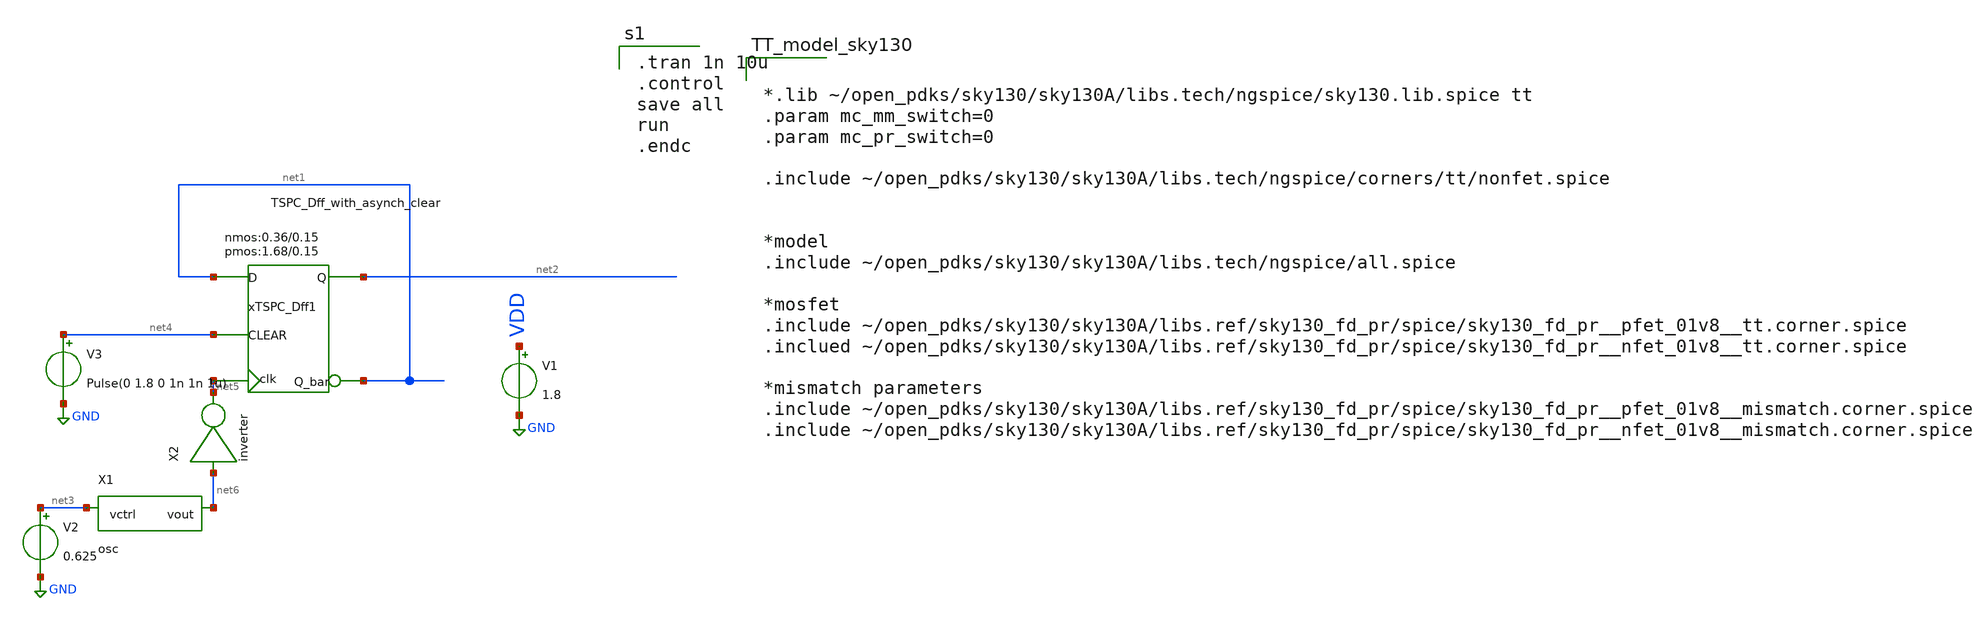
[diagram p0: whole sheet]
** sch_path: bf.sch
**.subckt bf
xTSPC_Dff1 net5 net1 net1 net2 net4 VDD GND TSPC_Dff_with_asynch_clear wnmos=0.36 lnmos=0.15
+ wpmos=1.68 lpmos=0.15 m=1
V1 VDD GND 1.8
X1 net3 net6 osc
V2 net3 GND 0.625
V3 net4 GND Pulse(0 1.8 0 1n 1n 1u)
X2 net6 net5 inverter
**** begin user architecture code

.tran 1n 10u
.control
save all
run
.endc


*.lib ~/open_pdks/sky130/sky130A/libs.tech/ngspice/sky130.lib.spice tt
.param mc_mm_switch=0
.param mc_pr_switch=0

.include ~/open_pdks/sky130/sky130A/libs.tech/ngspice/corners/tt/nonfet.spice


*model
.include ~/open_pdks/sky130/sky130A/libs.tech/ngspice/all.spice

*mosfet
.include ~/open_pdks/sky130/sky130A/libs.ref/sky130_fd_pr/spice/sky130_fd_pr__pfet_01v8__tt.corner.spice
.inclued ~/open_pdks/sky130/sky130A/libs.ref/sky130_fd_pr/spice/sky130_fd_pr__nfet_01v8__tt.corner.spice

*mismatch parameters
.include ~/open_pdks/sky130/sky130A/libs.ref/sky130_fd_pr/spice/sky130_fd_pr__pfet_01v8__mismatch.corner.spice
.include ~/open_pdks/sky130/sky130A/libs.ref/sky130_fd_pr/spice/sky130_fd_pr__nfet_01v8__mismatch.corner.spice

**** end user architecture code
**.ends

* expanding   symbol:  /home/cegrahul/Downloads/TSPC_Dff_with_asynch_clear.sym # of pins=5
** sym_path: TSPC_Dff_with_asynch_clear.sym
** sch_path: TSPC_Dff_with_asynch_clear.sch
.subckt TSPC_Dff_with_asynch_clear clk D Q_bar Q CLEAR VDDPIN VSSPIN       wnmos=0.36 lnmos=0.15
+  wpmos=1.68 lpmos=0.15
*.ipin D
*.ipin clk
*.opin Q
*.opin Q_bar
*.ipin CLEAR
XM1 net2 D VSSPIN VSSPIN sky130_fd_pr__nfet_01v8 L=lnmos W=wnmos nf=1 ad='int((nf+1)/2) * W/nf * 0.29'
+ as='int((nf+2)/2) * W/nf * 0.29' pd='2*int((nf+1)/2) * (W/nf + 0.29)' ps='2*int((nf+2)/2) * (W/nf + 0.29)'
+ nrd='0.29 / W' nrs='0.29 / W' sa=0 sb=0 sd=0 mult=1 m=1
XM2 net1 D VDDPIN VDDPIN sky130_fd_pr__pfet_01v8 L=lpmos W=wpmos nf=1 ad='int((nf+1)/2) * W/nf * 0.29'
+ as='int((nf+2)/2) * W/nf * 0.29' pd='2*int((nf+1)/2) * (W/nf + 0.29)' ps='2*int((nf+2)/2) * (W/nf + 0.29)'
+ nrd='0.29 / W' nrs='0.29 / W' sa=0 sb=0 sd=0 mult=1 m=1
XM3 net2 clk net1 VDDPIN sky130_fd_pr__pfet_01v8 L=lpmos W=wpmos nf=1 ad='int((nf+1)/2) * W/nf * 0.29'
+ as='int((nf+2)/2) * W/nf * 0.29' pd='2*int((nf+1)/2) * (W/nf + 0.29)' ps='2*int((nf+2)/2) * (W/nf + 0.29)'
+ nrd='0.29 / W' nrs='0.29 / W' sa=0 sb=0 sd=0 mult=1 m=1
XM4 net6 clk VSSPIN VSSPIN sky130_fd_pr__nfet_01v8 L=lnmos W=wnmos nf=1 ad='int((nf+1)/2) * W/nf * 0.29'
+ as='int((nf+2)/2) * W/nf * 0.29' pd='2*int((nf+1)/2) * (W/nf + 0.29)' ps='2*int((nf+2)/2) * (W/nf + 0.29)'
+ nrd='0.29 / W' nrs='0.29 / W' sa=0 sb=0 sd=0 mult=1 m=1
XM5 net7 clk VDDPIN VDDPIN sky130_fd_pr__pfet_01v8 L=lpmos W=wpmos nf=1 ad='int((nf+1)/2) * W/nf * 0.29'
+ as='int((nf+2)/2) * W/nf * 0.29' pd='2*int((nf+1)/2) * (W/nf + 0.29)' ps='2*int((nf+2)/2) * (W/nf + 0.29)'
+ nrd='0.29 / W' nrs='0.29 / W' sa=0 sb=0 sd=0 mult=1 m=1
XM6 net4 net5 VSSPIN VSSPIN sky130_fd_pr__nfet_01v8 L=0.50 W=0.42 nf=1 ad='int((nf+1)/2) * W/nf * 0.29'
+ as='int((nf+2)/2) * W/nf * 0.29' pd='2*int((nf+1)/2) * (W/nf + 0.29)' ps='2*int((nf+2)/2) * (W/nf + 0.29)'
+ nrd='0.29 / W' nrs='0.29 / W' sa=0 sb=0 sd=0 mult=1 m=1
XM7 net3 net5 VDDPIN VDDPIN sky130_fd_pr__pfet_01v8 L=lpmos W=wpmos nf=1 ad='int((nf+1)/2) * W/nf * 0.29'
+ as='int((nf+2)/2) * W/nf * 0.29' pd='2*int((nf+1)/2) * (W/nf + 0.29)' ps='2*int((nf+2)/2) * (W/nf + 0.29)'
+ nrd='0.29 / W' nrs='0.29 / W' sa=0 sb=0 sd=0 mult=1 m=1
XM9 net5 net2 net6 VSSPIN sky130_fd_pr__nfet_01v8 L=lnmos W=wnmos nf=1 ad='int((nf+1)/2) * W/nf * 0.29'
+ as='int((nf+2)/2) * W/nf * 0.29' pd='2*int((nf+1)/2) * (W/nf + 0.29)' ps='2*int((nf+2)/2) * (W/nf + 0.29)'
+ nrd='0.29 / W' nrs='0.29 / W' sa=0 sb=0 sd=0 mult=1 m=1
XM11 net3 clk net4 VSSPIN sky130_fd_pr__nfet_01v8 L=0.50 W=0.42 nf=1 ad='int((nf+1)/2) * W/nf * 0.29'
+ as='int((nf+2)/2) * W/nf * 0.29' pd='2*int((nf+1)/2) * (W/nf + 0.29)' ps='2*int((nf+2)/2) * (W/nf + 0.29)'
+ nrd='0.29 / W' nrs='0.29 / W' sa=0 sb=0 sd=0 mult=1 m=1
XM10 Q net3 VDDPIN VDDPIN sky130_fd_pr__pfet_01v8 L=lpmos W=wpmos nf=1 ad='int((nf+1)/2) * W/nf * 0.29'
+ as='int((nf+2)/2) * W/nf * 0.29' pd='2*int((nf+1)/2) * (W/nf + 0.29)' ps='2*int((nf+2)/2) * (W/nf + 0.29)'
+ nrd='0.29 / W' nrs='0.29 / W' sa=0 sb=0 sd=0 mult=1 m=1
XM13 Q net3 VSSPIN VSSPIN sky130_fd_pr__nfet_01v8 L=lnmos W=wnmos nf=1 ad='int((nf+1)/2) * W/nf * 0.29'
+ as='int((nf+2)/2) * W/nf * 0.29' pd='2*int((nf+1)/2) * (W/nf + 0.29)' ps='2*int((nf+2)/2) * (W/nf + 0.29)'
+ nrd='0.29 / W' nrs='0.29 / W' sa=0 sb=0 sd=0 mult=1 m=1
XM12 Q_bar Q VDDPIN VDDPIN sky130_fd_pr__pfet_01v8 L=lpmos W=wpmos nf=1 ad='int((nf+1)/2) * W/nf * 0.29'
+ as='int((nf+2)/2) * W/nf * 0.29' pd='2*int((nf+1)/2) * (W/nf + 0.29)' ps='2*int((nf+2)/2) * (W/nf + 0.29)'
+ nrd='0.29 / W' nrs='0.29 / W' sa=0 sb=0 sd=0 mult=1 m=1
XM17 Q_bar Q VSSPIN VSSPIN sky130_fd_pr__nfet_01v8 L=lnmos W=wnmos nf=1 ad='int((nf+1)/2) * W/nf * 0.29'
+ as='int((nf+2)/2) * W/nf * 0.29' pd='2*int((nf+1)/2) * (W/nf + 0.29)' ps='2*int((nf+2)/2) * (W/nf + 0.29)'
+ nrd='0.29 / W' nrs='0.29 / W' sa=0 sb=0 sd=0 mult=1 m=1
XM8 net5 CLEAR net7 VDDPIN sky130_fd_pr__pfet_01v8 L=lpmos W=wpmos nf=1 ad='int((nf+1)/2) * W/nf * 0.29'
+ as='int((nf+2)/2) * W/nf * 0.29' pd='2*int((nf+1)/2) * (W/nf + 0.29)' ps='2*int((nf+2)/2) * (W/nf + 0.29)'
+ nrd='0.29 / W' nrs='0.29 / W' sa=0 sb=0 sd=0 mult=1 m=1
XM14 net5 CLEAR VSSPIN VSSPIN sky130_fd_pr__nfet_01v8 L=lnmos W=wnmos nf=1 ad='int((nf+1)/2) * W/nf * 0.29'
+ as='int((nf+2)/2) * W/nf * 0.29' pd='2*int((nf+1)/2) * (W/nf + 0.29)' ps='2*int((nf+2)/2) * (W/nf + 0.29)'
+ nrd='0.29 / W' nrs='0.29 / W' sa=0 sb=0 sd=0 mult=1 m=1
.ends


* expanding   symbol:  /home/cegrahul/Desktop/SSCS/osc.sym # of pins=2
** sym_path: osc.sym
** sch_path: osc.sch
.subckt osc vctrl vout
*.ipin vctrl
*.opin vout
XM1 net1 vout net2 GND sky130_fd_pr__nfet_01v8 L=4 W=0.55 nf=1 ad='int((nf+1)/2) * W/nf * 0.29' as='int((nf+2)/2) * W/nf * 0.29'
+ pd='2*int((nf+1)/2) * (W/nf + 0.29)' ps='2*int((nf+2)/2) * (W/nf + 0.29)' nrd='0.29 / W' nrs='0.29 / W'
+ sa=0 sb=0 sd=0 mult=1 m=1
XM3 net1 vout net3 net4 sky130_fd_pr__pfet_01v8 L=4 W=1 nf=1 ad='int((nf+1)/2) * W/nf * 0.29' as='int((nf+2)/2) * W/nf * 0.29'
+ pd='2*int((nf+1)/2) * (W/nf + 0.29)' ps='2*int((nf+2)/2) * (W/nf + 0.29)' nrd='0.29 / W' nrs='0.29 / W'
+ sa=0 sb=0 sd=0 mult=1 m=1
XM19 net2 vout GND GND sky130_fd_pr__nfet_01v8 L=4 W=0.55 nf=1 ad='int((nf+1)/2) * W/nf * 0.29' as='int((nf+2)/2) * W/nf * 0.29'
+ pd='2*int((nf+1)/2) * (W/nf + 0.29)' ps='2*int((nf+2)/2) * (W/nf + 0.29)' nrd='0.29 / W' nrs='0.29 / W'
+ sa=0 sb=0 sd=0 mult=1 m=1
XM29 net3 vctrl net4 net4 sky130_fd_pr__pfet_01v8 L=2 W=1 nf=1 ad='int((nf+1)/2) * W/nf * 0.29' as='int((nf+2)/2) * W/nf * 0.29'
+ pd='2*int((nf+1)/2) * (W/nf + 0.29)' ps='2*int((nf+2)/2) * (W/nf + 0.29)' nrd='0.29 / W' nrs='0.29 / W'
+ sa=0 sb=0 sd=0 mult=1 m=1
V3 net4 GND 1.8
XM2 net5 net1 net6 GND sky130_fd_pr__nfet_01v8 L=4 W=0.55 nf=1 ad='int((nf+1)/2) * W/nf * 0.29' as='int((nf+2)/2) * W/nf * 0.29'
+ pd='2*int((nf+1)/2) * (W/nf + 0.29)' ps='2*int((nf+2)/2) * (W/nf + 0.29)' nrd='0.29 / W' nrs='0.29 / W'
+ sa=0 sb=0 sd=0 mult=1 m=1
XM4 net5 net1 net3 net4 sky130_fd_pr__pfet_01v8 L=4 W=1 nf=1 ad='int((nf+1)/2) * W/nf * 0.29' as='int((nf+2)/2) * W/nf * 0.29'
+ pd='2*int((nf+1)/2) * (W/nf + 0.29)' ps='2*int((nf+2)/2) * (W/nf + 0.29)' nrd='0.29 / W' nrs='0.29 / W'
+ sa=0 sb=0 sd=0 mult=1 m=1
XM5 net6 net1 GND GND sky130_fd_pr__nfet_01v8 L=4 W=0.55 nf=1 ad='int((nf+1)/2) * W/nf * 0.29' as='int((nf+2)/2) * W/nf * 0.29'
+ pd='2*int((nf+1)/2) * (W/nf + 0.29)' ps='2*int((nf+2)/2) * (W/nf + 0.29)' nrd='0.29 / W' nrs='0.29 / W'
+ sa=0 sb=0 sd=0 mult=1 m=1
XM6 net3 vctrl net4 net4 sky130_fd_pr__pfet_01v8 L=2 W=1 nf=1 ad='int((nf+1)/2) * W/nf * 0.29' as='int((nf+2)/2) * W/nf * 0.29'
+ pd='2*int((nf+1)/2) * (W/nf + 0.29)' ps='2*int((nf+2)/2) * (W/nf + 0.29)' nrd='0.29 / W' nrs='0.29 / W'
+ sa=0 sb=0 sd=0 mult=1 m=1
XM7 net7 net5 net8 GND sky130_fd_pr__nfet_01v8 L=4 W=0.55 nf=1 ad='int((nf+1)/2) * W/nf * 0.29' as='int((nf+2)/2) * W/nf * 0.29'
+ pd='2*int((nf+1)/2) * (W/nf + 0.29)' ps='2*int((nf+2)/2) * (W/nf + 0.29)' nrd='0.29 / W' nrs='0.29 / W'
+ sa=0 sb=0 sd=0 mult=1 m=1
XM8 net7 net5 net3 net4 sky130_fd_pr__pfet_01v8 L=4 W=1 nf=1 ad='int((nf+1)/2) * W/nf * 0.29' as='int((nf+2)/2) * W/nf * 0.29'
+ pd='2*int((nf+1)/2) * (W/nf + 0.29)' ps='2*int((nf+2)/2) * (W/nf + 0.29)' nrd='0.29 / W' nrs='0.29 / W'
+ sa=0 sb=0 sd=0 mult=1 m=1
XM9 net8 net5 GND GND sky130_fd_pr__nfet_01v8 L=4 W=0.55 nf=1 ad='int((nf+1)/2) * W/nf * 0.29' as='int((nf+2)/2) * W/nf * 0.29'
+ pd='2*int((nf+1)/2) * (W/nf + 0.29)' ps='2*int((nf+2)/2) * (W/nf + 0.29)' nrd='0.29 / W' nrs='0.29 / W'
+ sa=0 sb=0 sd=0 mult=1 m=1
XM10 net3 vctrl net4 net4 sky130_fd_pr__pfet_01v8 L=2 W=1 nf=1 ad='int((nf+1)/2) * W/nf * 0.29' as='int((nf+2)/2) * W/nf * 0.29'
+ pd='2*int((nf+1)/2) * (W/nf + 0.29)' ps='2*int((nf+2)/2) * (W/nf + 0.29)' nrd='0.29 / W' nrs='0.29 / W'
+ sa=0 sb=0 sd=0 mult=1 m=1
XM11 net9 net7 net10 GND sky130_fd_pr__nfet_01v8 L=4 W=0.55 nf=1 ad='int((nf+1)/2) * W/nf * 0.29' as='int((nf+2)/2) * W/nf * 0.29'
+ pd='2*int((nf+1)/2) * (W/nf + 0.29)' ps='2*int((nf+2)/2) * (W/nf + 0.29)' nrd='0.29 / W' nrs='0.29 / W'
+ sa=0 sb=0 sd=0 mult=1 m=1
XM12 net9 net7 net3 net4 sky130_fd_pr__pfet_01v8 L=4 W=1 nf=1 ad='int((nf+1)/2) * W/nf * 0.29' as='int((nf+2)/2) * W/nf * 0.29'
+ pd='2*int((nf+1)/2) * (W/nf + 0.29)' ps='2*int((nf+2)/2) * (W/nf + 0.29)' nrd='0.29 / W' nrs='0.29 / W'
+ sa=0 sb=0 sd=0 mult=1 m=1
XM13 net10 net7 GND GND sky130_fd_pr__nfet_01v8 L=4 W=0.55 nf=1 ad='int((nf+1)/2) * W/nf * 0.29' as='int((nf+2)/2) * W/nf * 0.29'
+ pd='2*int((nf+1)/2) * (W/nf + 0.29)' ps='2*int((nf+2)/2) * (W/nf + 0.29)' nrd='0.29 / W' nrs='0.29 / W'
+ sa=0 sb=0 sd=0 mult=1 m=1
XM14 net3 vctrl net4 net4 sky130_fd_pr__pfet_01v8 L=2 W=1 nf=1 ad='int((nf+1)/2) * W/nf * 0.29' as='int((nf+2)/2) * W/nf * 0.29'
+ pd='2*int((nf+1)/2) * (W/nf + 0.29)' ps='2*int((nf+2)/2) * (W/nf + 0.29)' nrd='0.29 / W' nrs='0.29 / W'
+ sa=0 sb=0 sd=0 mult=1 m=1
XM15 net11 net9 net12 GND sky130_fd_pr__nfet_01v8 L=4 W=0.55 nf=1 ad='int((nf+1)/2) * W/nf * 0.29' as='int((nf+2)/2) * W/nf * 0.29'
+ pd='2*int((nf+1)/2) * (W/nf + 0.29)' ps='2*int((nf+2)/2) * (W/nf + 0.29)' nrd='0.29 / W' nrs='0.29 / W'
+ sa=0 sb=0 sd=0 mult=1 m=1
XM16 net11 net9 net3 net4 sky130_fd_pr__pfet_01v8 L=4 W=1 nf=1 ad='int((nf+1)/2) * W/nf * 0.29' as='int((nf+2)/2) * W/nf * 0.29'
+ pd='2*int((nf+1)/2) * (W/nf + 0.29)' ps='2*int((nf+2)/2) * (W/nf + 0.29)' nrd='0.29 / W' nrs='0.29 / W'
+ sa=0 sb=0 sd=0 mult=1 m=1
XM17 net12 net9 GND GND sky130_fd_pr__nfet_01v8 L=4 W=0.55 nf=1 ad='int((nf+1)/2) * W/nf * 0.29' as='int((nf+2)/2) * W/nf * 0.29'
+ pd='2*int((nf+1)/2) * (W/nf + 0.29)' ps='2*int((nf+2)/2) * (W/nf + 0.29)' nrd='0.29 / W' nrs='0.29 / W'
+ sa=0 sb=0 sd=0 mult=1 m=1
XM18 net3 vctrl net4 net4 sky130_fd_pr__pfet_01v8 L=2 W=1 nf=1 ad='int((nf+1)/2) * W/nf * 0.29' as='int((nf+2)/2) * W/nf * 0.29'
+ pd='2*int((nf+1)/2) * (W/nf + 0.29)' ps='2*int((nf+2)/2) * (W/nf + 0.29)' nrd='0.29 / W' nrs='0.29 / W'
+ sa=0 sb=0 sd=0 mult=1 m=1
XM20 net13 net11 net14 GND sky130_fd_pr__nfet_01v8 L=4 W=0.55 nf=1 ad='int((nf+1)/2) * W/nf * 0.29' as='int((nf+2)/2) * W/nf * 0.29'
+ pd='2*int((nf+1)/2) * (W/nf + 0.29)' ps='2*int((nf+2)/2) * (W/nf + 0.29)' nrd='0.29 / W' nrs='0.29 / W'
+ sa=0 sb=0 sd=0 mult=1 m=1
XM21 net13 net11 net3 net4 sky130_fd_pr__pfet_01v8 L=4 W=1 nf=1 ad='int((nf+1)/2) * W/nf * 0.29' as='int((nf+2)/2) * W/nf * 0.29'
+ pd='2*int((nf+1)/2) * (W/nf + 0.29)' ps='2*int((nf+2)/2) * (W/nf + 0.29)' nrd='0.29 / W' nrs='0.29 / W'
+ sa=0 sb=0 sd=0 mult=1 m=1
XM22 net14 net11 GND GND sky130_fd_pr__nfet_01v8 L=4 W=0.55 nf=1 ad='int((nf+1)/2) * W/nf * 0.29' as='int((nf+2)/2) * W/nf * 0.29'
+ pd='2*int((nf+1)/2) * (W/nf + 0.29)' ps='2*int((nf+2)/2) * (W/nf + 0.29)' nrd='0.29 / W' nrs='0.29 / W'
+ sa=0 sb=0 sd=0 mult=1 m=1
XM23 net3 vctrl net4 net4 sky130_fd_pr__pfet_01v8 L=2 W=1 nf=1 ad='int((nf+1)/2) * W/nf * 0.29' as='int((nf+2)/2) * W/nf * 0.29'
+ pd='2*int((nf+1)/2) * (W/nf + 0.29)' ps='2*int((nf+2)/2) * (W/nf + 0.29)' nrd='0.29 / W' nrs='0.29 / W'
+ sa=0 sb=0 sd=0 mult=1 m=1
XM24 net15 net13 net16 GND sky130_fd_pr__nfet_01v8 L=4 W=0.55 nf=1 ad='int((nf+1)/2) * W/nf * 0.29' as='int((nf+2)/2) * W/nf * 0.29'
+ pd='2*int((nf+1)/2) * (W/nf + 0.29)' ps='2*int((nf+2)/2) * (W/nf + 0.29)' nrd='0.29 / W' nrs='0.29 / W'
+ sa=0 sb=0 sd=0 mult=1 m=1
XM25 net15 net13 net3 net4 sky130_fd_pr__pfet_01v8 L=4 W=1 nf=1 ad='int((nf+1)/2) * W/nf * 0.29' as='int((nf+2)/2) * W/nf * 0.29'
+ pd='2*int((nf+1)/2) * (W/nf + 0.29)' ps='2*int((nf+2)/2) * (W/nf + 0.29)' nrd='0.29 / W' nrs='0.29 / W'
+ sa=0 sb=0 sd=0 mult=1 m=1
XM26 net16 net13 GND GND sky130_fd_pr__nfet_01v8 L=4 W=0.55 nf=1 ad='int((nf+1)/2) * W/nf * 0.29' as='int((nf+2)/2) * W/nf * 0.29'
+ pd='2*int((nf+1)/2) * (W/nf + 0.29)' ps='2*int((nf+2)/2) * (W/nf + 0.29)' nrd='0.29 / W' nrs='0.29 / W'
+ sa=0 sb=0 sd=0 mult=1 m=1
XM27 net3 vctrl net4 net4 sky130_fd_pr__pfet_01v8 L=2 W=1 nf=1 ad='int((nf+1)/2) * W/nf * 0.29' as='int((nf+2)/2) * W/nf * 0.29'
+ pd='2*int((nf+1)/2) * (W/nf + 0.29)' ps='2*int((nf+2)/2) * (W/nf + 0.29)' nrd='0.29 / W' nrs='0.29 / W'
+ sa=0 sb=0 sd=0 mult=1 m=1
XM28 net17 net15 net18 GND sky130_fd_pr__nfet_01v8 L=4 W=0.55 nf=1 ad='int((nf+1)/2) * W/nf * 0.29' as='int((nf+2)/2) * W/nf * 0.29'
+ pd='2*int((nf+1)/2) * (W/nf + 0.29)' ps='2*int((nf+2)/2) * (W/nf + 0.29)' nrd='0.29 / W' nrs='0.29 / W'
+ sa=0 sb=0 sd=0 mult=1 m=1
XM30 net17 net15 net3 net4 sky130_fd_pr__pfet_01v8 L=4 W=1 nf=1 ad='int((nf+1)/2) * W/nf * 0.29' as='int((nf+2)/2) * W/nf * 0.29'
+ pd='2*int((nf+1)/2) * (W/nf + 0.29)' ps='2*int((nf+2)/2) * (W/nf + 0.29)' nrd='0.29 / W' nrs='0.29 / W'
+ sa=0 sb=0 sd=0 mult=1 m=1
XM31 net18 net15 GND GND sky130_fd_pr__nfet_01v8 L=4 W=0.55 nf=1 ad='int((nf+1)/2) * W/nf * 0.29' as='int((nf+2)/2) * W/nf * 0.29'
+ pd='2*int((nf+1)/2) * (W/nf + 0.29)' ps='2*int((nf+2)/2) * (W/nf + 0.29)' nrd='0.29 / W' nrs='0.29 / W'
+ sa=0 sb=0 sd=0 mult=1 m=1
XM32 net3 vctrl net4 net4 sky130_fd_pr__pfet_01v8 L=2 W=1 nf=1 ad='int((nf+1)/2) * W/nf * 0.29' as='int((nf+2)/2) * W/nf * 0.29'
+ pd='2*int((nf+1)/2) * (W/nf + 0.29)' ps='2*int((nf+2)/2) * (W/nf + 0.29)' nrd='0.29 / W' nrs='0.29 / W'
+ sa=0 sb=0 sd=0 mult=1 m=1
XM33 vout net17 net19 GND sky130_fd_pr__nfet_01v8 L=4 W=0.55 nf=1 ad='int((nf+1)/2) * W/nf * 0.29' as='int((nf+2)/2) * W/nf * 0.29'
+ pd='2*int((nf+1)/2) * (W/nf + 0.29)' ps='2*int((nf+2)/2) * (W/nf + 0.29)' nrd='0.29 / W' nrs='0.29 / W'
+ sa=0 sb=0 sd=0 mult=1 m=1
XM34 vout net17 net3 net4 sky130_fd_pr__pfet_01v8 L=4 W=1 nf=1 ad='int((nf+1)/2) * W/nf * 0.29' as='int((nf+2)/2) * W/nf * 0.29'
+ pd='2*int((nf+1)/2) * (W/nf + 0.29)' ps='2*int((nf+2)/2) * (W/nf + 0.29)' nrd='0.29 / W' nrs='0.29 / W'
+ sa=0 sb=0 sd=0 mult=1 m=1
XM35 net19 net17 GND GND sky130_fd_pr__nfet_01v8 L=4 W=0.55 nf=1 ad='int((nf+1)/2) * W/nf * 0.29' as='int((nf+2)/2) * W/nf * 0.29'
+ pd='2*int((nf+1)/2) * (W/nf + 0.29)' ps='2*int((nf+2)/2) * (W/nf + 0.29)' nrd='0.29 / W' nrs='0.29 / W'
+ sa=0 sb=0 sd=0 mult=1 m=1
XM36 net3 vctrl net4 net4 sky130_fd_pr__pfet_01v8 L=2 W=1 nf=1 ad='int((nf+1)/2) * W/nf * 0.29' as='int((nf+2)/2) * W/nf * 0.29'
+ pd='2*int((nf+1)/2) * (W/nf + 0.29)' ps='2*int((nf+2)/2) * (W/nf + 0.29)' nrd='0.29 / W' nrs='0.29 / W'
+ sa=0 sb=0 sd=0 mult=1 m=1
.ends


* expanding   symbol:  /home/cegrahul/Desktop/SSCS/inverter.sym # of pins=2
** sym_path: inverter.sym
** sch_path: inverter.sch
.subckt inverter vin vout
*.ipin vin
*.opin vout
XM2 vout vin net1 net1 sky130_fd_pr__pfet_01v8 L=0.15 W=1.68 nf=1 ad='int((nf+1)/2) * W/nf * 0.29' as='int((nf+2)/2) * W/nf * 0.29'
+ pd='2*int((nf+1)/2) * (W/nf + 0.29)' ps='2*int((nf+2)/2) * (W/nf + 0.29)' nrd='0.29 / W' nrs='0.29 / W'
+ sa=0 sb=0 sd=0 mult=1 m=1
XM3 vout vin GND GND sky130_fd_pr__nfet_01v8 L=0.15 W=0.36 nf=1 ad='int((nf+1)/2) * W/nf * 0.29' as='int((nf+2)/2) * W/nf * 0.29'
+ pd='2*int((nf+1)/2) * (W/nf + 0.29)' ps='2*int((nf+2)/2) * (W/nf + 0.29)' nrd='0.29 / W' nrs='0.29 / W'
+ sa=0 sb=0 sd=0 mult=1 m=1
V3 net1 GND 1.8
.ends

.GLOBAL GND
.end
